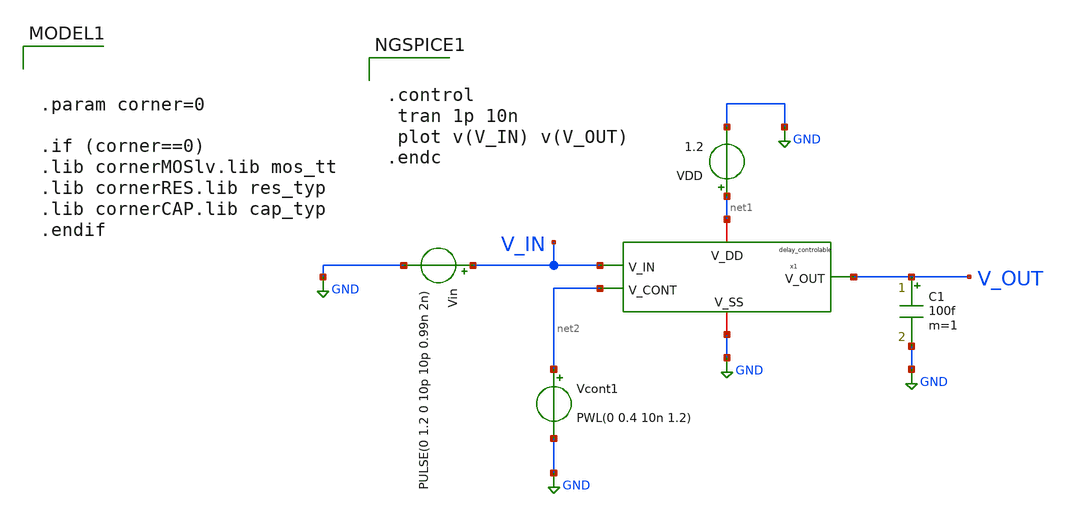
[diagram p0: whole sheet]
** sch_path: others/clemen/testbench.sch
**.subckt testbench
VDD net1 GND 1.2
Vin V_IN GND PULSE(0 1.2 0 10p 10p 0.99n 2n)
C1 V_OUT GND 100f m=1
x1 net1 V_OUT V_IN net2 GND delay_controlable
Vcont1 net2 GND PWL(0 0.4 10n 1.2)
**** begin user architecture code


.param corner=0

.if (corner==0)
.lib cornerMOSlv.lib mos_tt
.lib cornerRES.lib res_typ
.lib cornerCAP.lib cap_typ
.endif



.control
 tran 1p 10n
 plot v(V_IN) v(V_OUT)
.endc


**** end user architecture code
**.ends

* expanding   symbol:  /foss/designs/DLL/2026/clemen/delay_controlable.sym # of pins=5
** sym_path: others/clemen/delay_controlable.sym
** sch_path: others/clemen/delay_controlable.sch
.subckt delay_controlable V_DD V_OUT V_IN V_CONT V_SS
*.iopin V_DD
*.iopin V_SS
*.ipin V_IN
*.ipin V_CONT
*.opin V_OUT
XM1 V_OUT V_IN net3 V_SS sg13_lv_nmos w=2u l=0.13u ng=1 m=1 mm_ok=1
XM2 net3 V_CONT V_SS V_SS sg13_lv_nmos w=5u l=0.16u ng=1 m=1 mm_ok=1
XM3 net1 V_CONT V_SS V_SS sg13_lv_nmos w=2u l=0.25u ng=1 m=1 mm_ok=1
XM4 V_OUT V_IN net2 V_DD sg13_lv_pmos w=5u l=0.13u ng=1 m=1 mm_ok=1
XM5 net2 net1 V_DD V_DD sg13_lv_pmos w=5u l=0.16u ng=1 m=1 mm_ok=1
XM6 net1 net1 V_DD V_DD sg13_lv_pmos w=2.24u l=0.13u ng=1 m=1 mm_ok=1
.ends

.GLOBAL GND
.end
